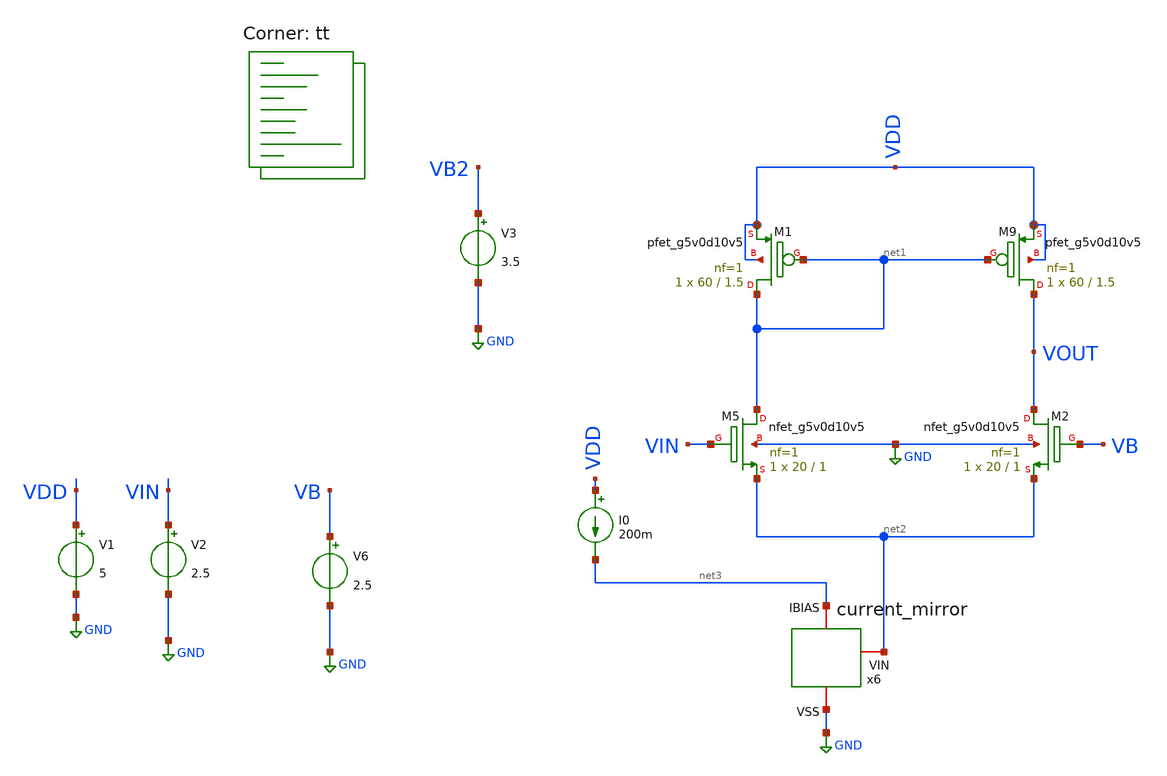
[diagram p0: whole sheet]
** sch_path: amplifiers/differencial_stage_amps/single_output/active_load/diferential_stage.sch
**.subckt diferential_stage
V1 VDD GND 5
V2 VIN GND 2.5
V6 VB GND 2.5
V3 VB2 GND 3.5
XM9 VOUT net1 VDD VDD sky130_fd_pr__pfet_g5v0d10v5 L=1.5 W=60 nf=1 ad='int((1 + 1)/2) * 60 / 1 * 0.29'
+ as='int((1 + 2)/2) * 60 / 1 * 0.29' pd='2*int((1 + 1)/2) * (60 / 1 + 0.29)' ps='2*int((1 + 2)/2) * (60 / 1 + 0.29)'
+ nrd='0.29 / 60 ' nrs='0.29 / 60 ' sa=0 sb=0 sd=0 mult=1 m=1
XM1 net1 net1 VDD VDD sky130_fd_pr__pfet_g5v0d10v5 L=1.5 W=60 nf=1 ad='int((1 + 1)/2) * 60 / 1 * 0.29'
+ as='int((1 + 2)/2) * 60 / 1 * 0.29' pd='2*int((1 + 1)/2) * (60 / 1 + 0.29)' ps='2*int((1 + 2)/2) * (60 / 1 + 0.29)'
+ nrd='0.29 / 60 ' nrs='0.29 / 60 ' sa=0 sb=0 sd=0 mult=1 m=1
XM5 net1 VIN net2 GND sky130_fd_pr__nfet_g5v0d10v5 L=1 W=20 nf=1 ad='int((1 + 1)/2) * 20 / 1 * 0.29'
+ as='int((1 + 2)/2) * 20 / 1 * 0.29' pd='2*int((1 + 1)/2) * (20 / 1 + 0.29)' ps='2*int((1 + 2)/2) * (20 / 1 + 0.29)'
+ nrd='0.29 / 20 ' nrs='0.29 / 20 ' sa=0 sb=0 sd=0 mult=1 m=1
XM2 VOUT VB net2 GND sky130_fd_pr__nfet_g5v0d10v5 L=1 W=20 nf=1 ad='int((1 + 1)/2) * 20 / 1 * 0.29' as='int((1 + 2)/2) * 20 / 1 * 0.29'
+ pd='2*int((1 + 1)/2) * (20 / 1 + 0.29)' ps='2*int((1 + 2)/2) * (20 / 1 + 0.29)' nrd='0.29 / 20 ' nrs='0.29 / 20 '
+ sa=0 sb=0 sd=0 mult=1 m=1
x6 net3 GND net2 current_mirror
I0 VDD net3 200m
**** begin user architecture code

**************************************************************
**************************************************************
**************************************************************
**************************************************************
**************************************************************
*LIBs*********************************************************
**************************************************************
**************************************************************
**************************************************************
**************************************************************
**************************************************************
*.lib $::SKYWATER_MODELS/sky130.lib.spice tt
* chose the corners in the corner file
* tt_mm for mismatch
* ss ff sf fs standart corners
* ll hh lh hl capacitor and resistors corners
* mc for total process variation including corners
**************************************************************
**************************************************************
**************************************************************
**************************************************************
**************************************************************
*Corners/montecarlo options***********************************
**************************************************************
**************************************************************
**************************************************************
**************************************************************
**************************************************************
.TEMP 27
**************************************************************
**************************************************************
**************************************************************
**************************************************************
*SIMULATION and Plots*****************************************
**************************************************************
**************************************************************
**************************************************************
**************************************************************
.control
save all
dc V2 0 5 0.01
*dc simulation
plot v(VOUT) v(VIN) deriv(v(VOUT))

.endc

.lib $::SKYWATER_MODELS/sky130.lib.spice tt
**** end user architecture code
**.ends

* expanding   symbol:
*+  /home/vasco/Desktop/sky130A/amplifiers/current_mirrors/lower_vt_current_mirror/current_mirror.sym # of pins=3
** sym_path: amplifiers/current_mirrors/lower_vt_current_mirror/current_mirror.sym
** sch_path: amplifiers/current_mirrors/lower_vt_current_mirror/current_mirror.sch
.subckt current_mirror IBIAS VSS VIN
*.iopin IBIAS
*.iopin VSS
*.iopin VIN
XM5 net1 IBIAS VSS VSS sky130_fd_pr__nfet_g5v0d10v5 L=0.7 W=50 nf=1 ad='int((1 + 1)/2) * 50 / 1 * 0.29'
+ as='int((1 + 2)/2) * 50 / 1 * 0.29' pd='2*int((1 + 1)/2) * (50 / 1 + 0.29)' ps='2*int((1 + 2)/2) * (50 / 1 + 0.29)'
+ nrd='0.29 / 50 ' nrs='0.29 / 50 ' sa=0 sb=0 sd=0 mult=1 m=1
XM1 net2 IBIAS VSS VSS sky130_fd_pr__nfet_g5v0d10v5 L=0.7 W=50 nf=1 ad='int((1 + 1)/2) * 50 / 1 * 0.29'
+ as='int((1 + 2)/2) * 50 / 1 * 0.29' pd='2*int((1 + 1)/2) * (50 / 1 + 0.29)' ps='2*int((1 + 2)/2) * (50 / 1 + 0.29)'
+ nrd='0.29 / 50 ' nrs='0.29 / 50 ' sa=0 sb=0 sd=0 mult=1 m=1
XM2 IBIAS VB1 net1 VSS sky130_fd_pr__nfet_g5v0d10v5 L=0.7 W=50 nf=1 ad='int((1 + 1)/2) * 50 / 1 * 0.29'
+ as='int((1 + 2)/2) * 50 / 1 * 0.29' pd='2*int((1 + 1)/2) * (50 / 1 + 0.29)' ps='2*int((1 + 2)/2) * (50 / 1 + 0.29)'
+ nrd='0.29 / 50 ' nrs='0.29 / 50 ' sa=0 sb=0 sd=0 mult=1 m=1
XM3 VIN VB1 net2 VSS sky130_fd_pr__nfet_g5v0d10v5 L=0.7 W=50 nf=1 ad='int((1 + 1)/2) * 50 / 1 * 0.29'
+ as='int((1 + 2)/2) * 50 / 1 * 0.29' pd='2*int((1 + 1)/2) * (50 / 1 + 0.29)' ps='2*int((1 + 2)/2) * (50 / 1 + 0.29)'
+ nrd='0.29 / 50 ' nrs='0.29 / 50 ' sa=0 sb=0 sd=0 mult=1 m=1
I0 net3 VB1 200u
V1 net3 VSS 5
XM4 VB1 VB1 net4 VSS sky130_fd_pr__nfet_g5v0d10v5 L=2 W=10 nf=1 ad='int((1 + 1)/2) * 10 / 1 * 0.29' as='int((1 + 2)/2) * 10 / 1 * 0.29'
+ pd='2*int((1 + 1)/2) * (10 / 1 + 0.29)' ps='2*int((1 + 2)/2) * (10 / 1 + 0.29)' nrd='0.29 / 10 ' nrs='0.29 / 10 '
+ sa=0 sb=0 sd=0 mult=1 m=1
XM6 net4 VB1 VSS VSS sky130_fd_pr__nfet_g5v0d10v5 L=2 W=10 nf=1 ad='int((1 + 1)/2) * 10 / 1 * 0.29' as='int((1 + 2)/2) * 10 / 1 * 0.29'
+ pd='2*int((1 + 1)/2) * (10 / 1 + 0.29)' ps='2*int((1 + 2)/2) * (10 / 1 + 0.29)' nrd='0.29 / 10 ' nrs='0.29 / 10 '
+ sa=0 sb=0 sd=0 mult=1 m=1
.ends

.GLOBAL GND
.end
